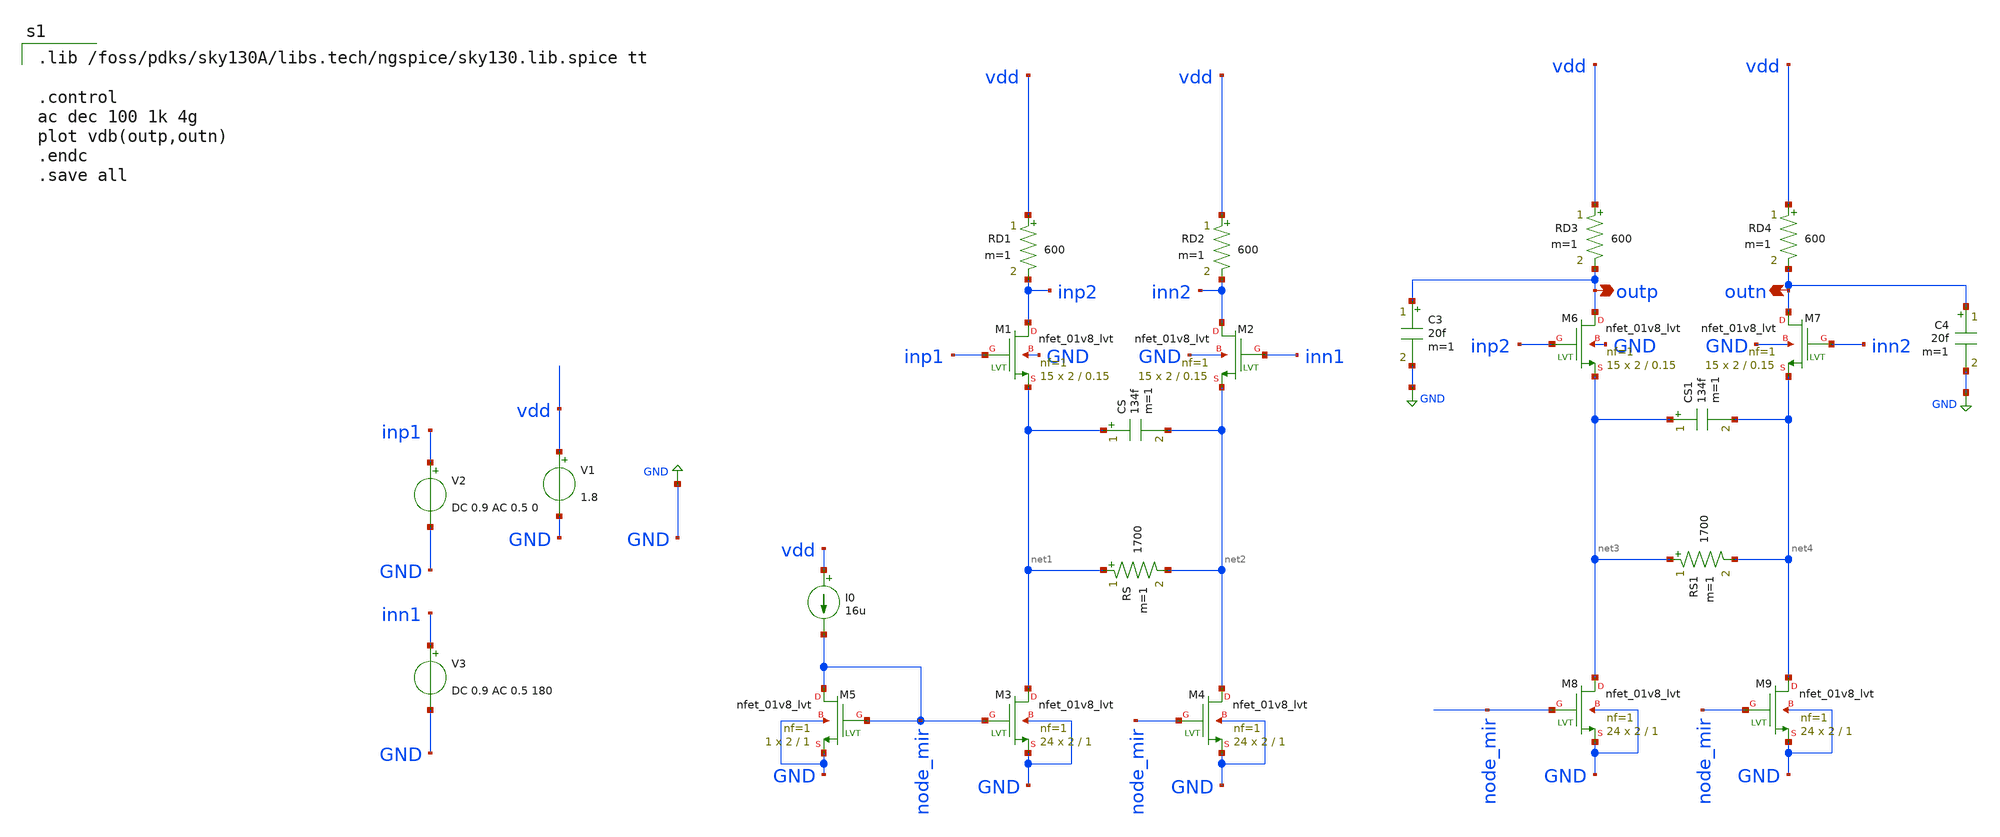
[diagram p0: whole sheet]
** sch_path: CTLE/ctle_two_stage.sch
**.subckt ctle_two_stage outp outn
*.opin outp
*.opin outn
V1 vdd GND 1.8
V2 inp1 GND DC 0.9 AC 0.5 0
V3 inn1 GND DC 0.9 AC 0.5 180
XM1 inp2 inp1 net1 GND sky130_fd_pr__nfet_01v8_lvt L=0.15 W=2 nf=1 ad='int((nf+1)/2) * W/nf * 0.29' as='int((nf+2)/2) * W/nf * 0.29'
+ pd='2*int((nf+1)/2) * (W/nf + 0.29)' ps='2*int((nf+2)/2) * (W/nf + 0.29)' nrd='0.29 / W' nrs='0.29 / W'
+ sa=0 sb=0 sd=0 mult=15 m=15
XM2 inn2 inn1 net2 GND sky130_fd_pr__nfet_01v8_lvt L=0.15 W=2 nf=1 ad='int((nf+1)/2) * W/nf * 0.29' as='int((nf+2)/2) * W/nf * 0.29'
+ pd='2*int((nf+1)/2) * (W/nf + 0.29)' ps='2*int((nf+2)/2) * (W/nf + 0.29)' nrd='0.29 / W' nrs='0.29 / W'
+ sa=0 sb=0 sd=0 mult=15 m=15
I0 vdd node_mir 16u
XM3 net1 node_mir GND GND sky130_fd_pr__nfet_01v8_lvt L=1 W=2 nf=1 ad='int((nf+1)/2) * W/nf * 0.29' as='int((nf+2)/2) * W/nf * 0.29'
+ pd='2*int((nf+1)/2) * (W/nf + 0.29)' ps='2*int((nf+2)/2) * (W/nf + 0.29)' nrd='0.29 / W' nrs='0.29 / W'
+ sa=0 sb=0 sd=0 mult=24 m=24
XM4 net2 node_mir GND GND sky130_fd_pr__nfet_01v8_lvt L=1 W=2 nf=1 ad='int((nf+1)/2) * W/nf * 0.29' as='int((nf+2)/2) * W/nf * 0.29'
+ pd='2*int((nf+1)/2) * (W/nf + 0.29)' ps='2*int((nf+2)/2) * (W/nf + 0.29)' nrd='0.29 / W' nrs='0.29 / W'
+ sa=0 sb=0 sd=0 mult=24 m=24
XM5 node_mir node_mir GND GND sky130_fd_pr__nfet_01v8_lvt L=1 W=2 nf=1 ad='int((nf+1)/2) * W/nf * 0.29'
+ as='int((nf+2)/2) * W/nf * 0.29' pd='2*int((nf+1)/2) * (W/nf + 0.29)' ps='2*int((nf+2)/2) * (W/nf + 0.29)'
+ nrd='0.29 / W' nrs='0.29 / W' sa=0 sb=0 sd=0 mult=1 m=1
RD1 vdd inp2 600 m=1
RD2 vdd inn2 600 m=1
CS net1 net2 134f m=1
RS net1 net2 1700 m=1
XM6 outp inp2 net3 GND sky130_fd_pr__nfet_01v8_lvt L=0.15 W=2 nf=1 ad='int((nf+1)/2) * W/nf * 0.29' as='int((nf+2)/2) * W/nf * 0.29'
+ pd='2*int((nf+1)/2) * (W/nf + 0.29)' ps='2*int((nf+2)/2) * (W/nf + 0.29)' nrd='0.29 / W' nrs='0.29 / W'
+ sa=0 sb=0 sd=0 mult=15 m=15
XM7 outn inn2 net4 GND sky130_fd_pr__nfet_01v8_lvt L=0.15 W=2 nf=1 ad='int((nf+1)/2) * W/nf * 0.29' as='int((nf+2)/2) * W/nf * 0.29'
+ pd='2*int((nf+1)/2) * (W/nf + 0.29)' ps='2*int((nf+2)/2) * (W/nf + 0.29)' nrd='0.29 / W' nrs='0.29 / W'
+ sa=0 sb=0 sd=0 mult=15 m=15
XM8 net3 node_mir GND GND sky130_fd_pr__nfet_01v8_lvt L=1 W=2 nf=1 ad='int((nf+1)/2) * W/nf * 0.29' as='int((nf+2)/2) * W/nf * 0.29'
+ pd='2*int((nf+1)/2) * (W/nf + 0.29)' ps='2*int((nf+2)/2) * (W/nf + 0.29)' nrd='0.29 / W' nrs='0.29 / W'
+ sa=0 sb=0 sd=0 mult=24 m=24
XM9 net4 node_mir GND GND sky130_fd_pr__nfet_01v8_lvt L=1 W=2 nf=1 ad='int((nf+1)/2) * W/nf * 0.29' as='int((nf+2)/2) * W/nf * 0.29'
+ pd='2*int((nf+1)/2) * (W/nf + 0.29)' ps='2*int((nf+2)/2) * (W/nf + 0.29)' nrd='0.29 / W' nrs='0.29 / W'
+ sa=0 sb=0 sd=0 mult=24 m=24
RD3 vdd outp 600 m=1
RD4 vdd outn 600 m=1
CS1 net3 net4 134f m=1
RS1 net3 net4 1700 m=1
C3 outp GND 20f m=1
C4 outn GND 20f m=1
**** begin user architecture code

.lib /foss/pdks/sky130A/libs.tech/ngspice/sky130.lib.spice tt

.control
ac dec 100 1k 4g
plot vdb(outp,outn)
.endc
.save all


**** end user architecture code
**.ends
.GLOBAL GND
.end
